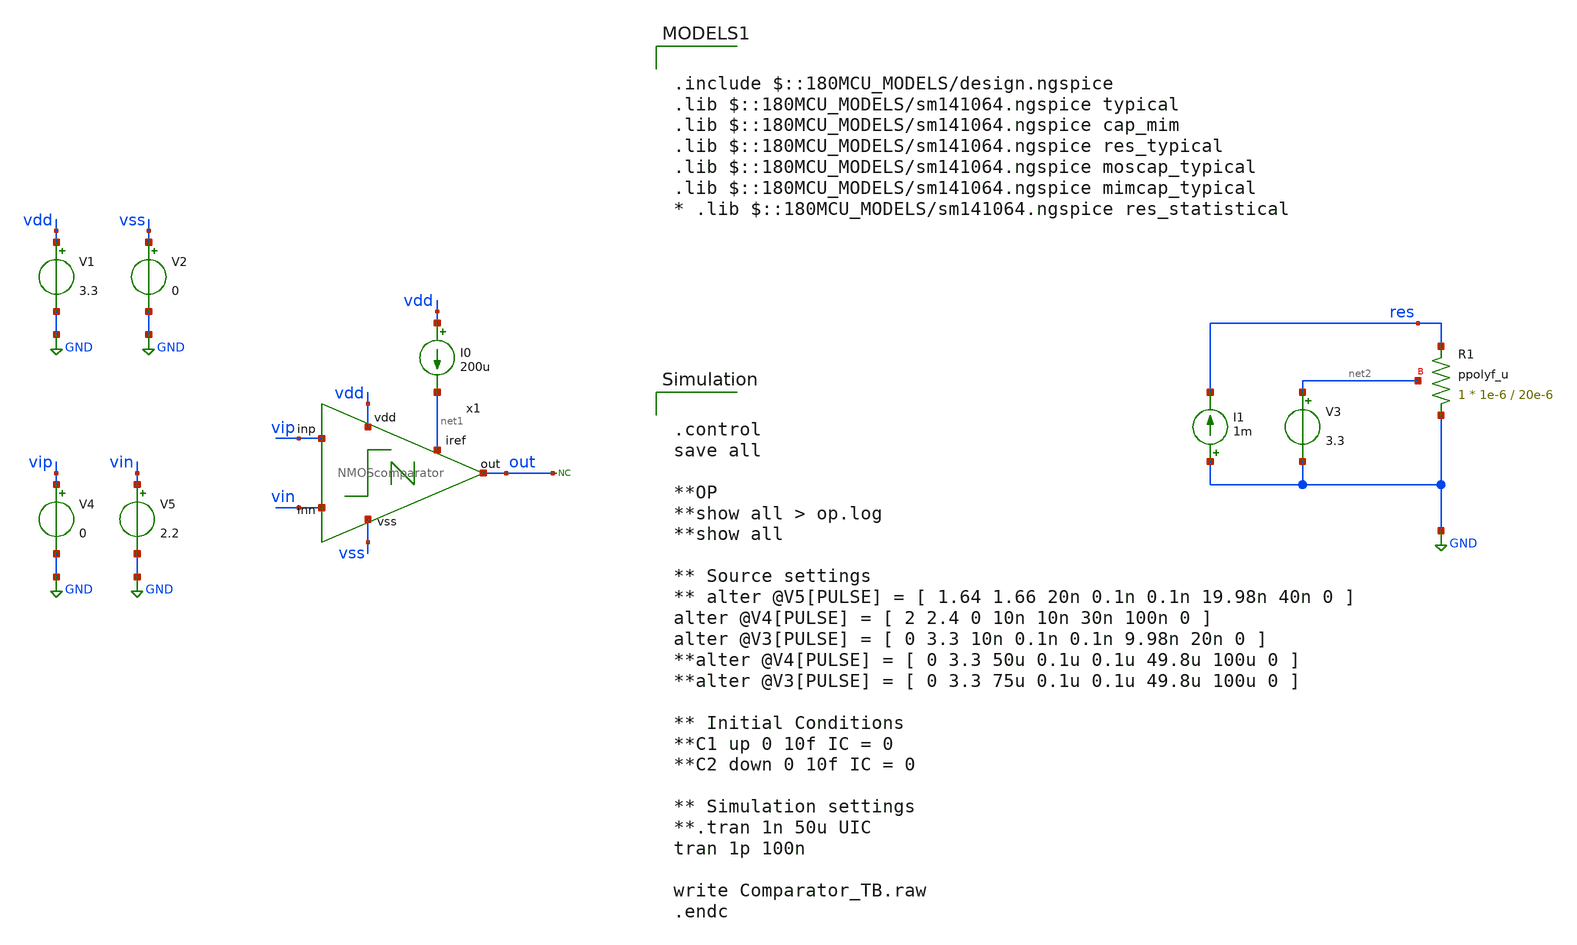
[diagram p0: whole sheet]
** sch_path: designs/libs/qw_core_analog/Comparator_TB.sch
**.subckt Comparator_TB
V1 vdd GND 3.3
V2 vss GND 0
* noconn out
V4 vip GND 0
V5 vin GND 2.2
x1 vdd vip out vin net1 vss NMOScomparator
I0 vdd net1 200u
V3 net2 GND 3.3
I1 GND res 1m
XR1 GND res net2 ppolyf_u r_width=1e-6 r_length=20e-6 m=1
**** begin user architecture code


.control
save all

**OP
**show all > op.log
**show all

** Source settings
** alter @V5[PULSE] = [ 1.64 1.66 20n 0.1n 0.1n 19.98n 40n 0 ]
alter @V4[PULSE] = [ 2 2.4 0 10n 10n 30n 100n 0 ]
alter @V3[PULSE] = [ 0 3.3 10n 0.1n 0.1n 9.98n 20n 0 ]
**alter @V4[PULSE] = [ 0 3.3 50u 0.1u 0.1u 49.8u 100u 0 ]
**alter @V3[PULSE] = [ 0 3.3 75u 0.1u 0.1u 49.8u 100u 0 ]

** Initial Conditions
**C1 up 0 10f IC = 0
**C2 down 0 10f IC = 0

** Simulation settings
**.tran 1n 50u UIC
tran 1p 100n

write Comparator_TB.raw
.endc



.include $::180MCU_MODELS/design.ngspice
.lib $::180MCU_MODELS/sm141064.ngspice typical
.lib $::180MCU_MODELS/sm141064.ngspice cap_mim
.lib $::180MCU_MODELS/sm141064.ngspice res_typical
.lib $::180MCU_MODELS/sm141064.ngspice moscap_typical
.lib $::180MCU_MODELS/sm141064.ngspice mimcap_typical
* .lib $::180MCU_MODELS/sm141064.ngspice res_statistical

**** end user architecture code
**.ends
.GLOBAL GND
.end
